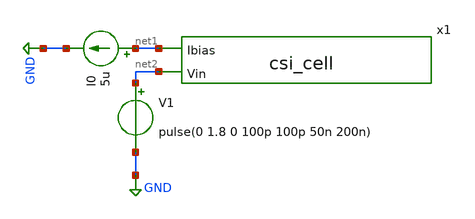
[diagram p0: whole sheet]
** sch_path: csi_cell/sim/tb_csi_cell.sch
**.subckt tb_csi_cell
x1 net1 net2 csi_cell
I0 net1 GND 5u
V1 net2 GND pulse(0 1.8 0 100p 100p 50n 200n)
**** begin user architecture code



.lib /foss/pdks/sky130A/libs.tech/ngspice/sky130.lib.spice tt
.tran 0.1n 400n

.save all

**** end user architecture code
**.ends

* expanding   symbol:  /headless/pulse-generator/csi_cell/csi_cell.sym # of pins=2
** sym_path: csi_cell/csi_cell.sym
** sch_path: csi_cell/csi_cell.sch
.subckt csi_cell Ibias Vin
*.ipin Vin
*.ipin Ibias
XM2 Vout Vin net2 GND sky130_fd_pr__nfet_01v8 L=0.15 W=1 nf=1 ad='int((1 + 1)/2) * 1 / 1 * 0.29' as='int((1 + 2)/2) * 1 / 1 * 0.29'
+ pd='2*int((1 + 1)/2) * (1 / 1 + 0.29)' ps='2*int((1 + 2)/2) * (1 / 1 + 0.29)' nrd='0.29 / 1 ' nrs='0.29 / 1 '
+ sa=0 sb=0 sd=0 mult=1 m=1
XM3 net2 Ibias GND GND sky130_fd_pr__nfet_01v8 L=0.5 W=1 nf=1 ad='int((1 + 1)/2) * 1 / 1 * 0.29' as='int((1 + 2)/2) * 1 / 1 * 0.29'
+ pd='2*int((1 + 1)/2) * (1 / 1 + 0.29)' ps='2*int((1 + 2)/2) * (1 / 1 + 0.29)' nrd='0.29 / 1 ' nrs='0.29 / 1 '
+ sa=0 sb=0 sd=0 mult=1 m=1
XM4 Vout Vin net1 VDD sky130_fd_pr__pfet_01v8 L=0.15 W=2 nf=1 ad='int((1 + 1)/2) * 2 / 1 * 0.29' as='int((1 + 2)/2) * 2 / 1 * 0.29'
+ pd='2*int((1 + 1)/2) * (2 / 1 + 0.29)' ps='2*int((1 + 2)/2) * (2 / 1 + 0.29)' nrd='0.29 / 2 ' nrs='0.29 / 2 '
+ sa=0 sb=0 sd=0 mult=1 m=1
XM5 net1 Ibias VDD VDD sky130_fd_pr__pfet_01v8 L=0.5 W=1 nf=1 ad='int((1 + 1)/2) * 1 / 1 * 0.29' as='int((1 + 2)/2) * 1 / 1 * 0.29'
+ pd='2*int((1 + 1)/2) * (1 / 1 + 0.29)' ps='2*int((1 + 2)/2) * (1 / 1 + 0.29)' nrd='0.29 / 1 ' nrs='0.29 / 1 '
+ sa=0 sb=0 sd=0 mult=1 m=1
V1 VDD GND 1.8
.ends

.GLOBAL GND
.end
